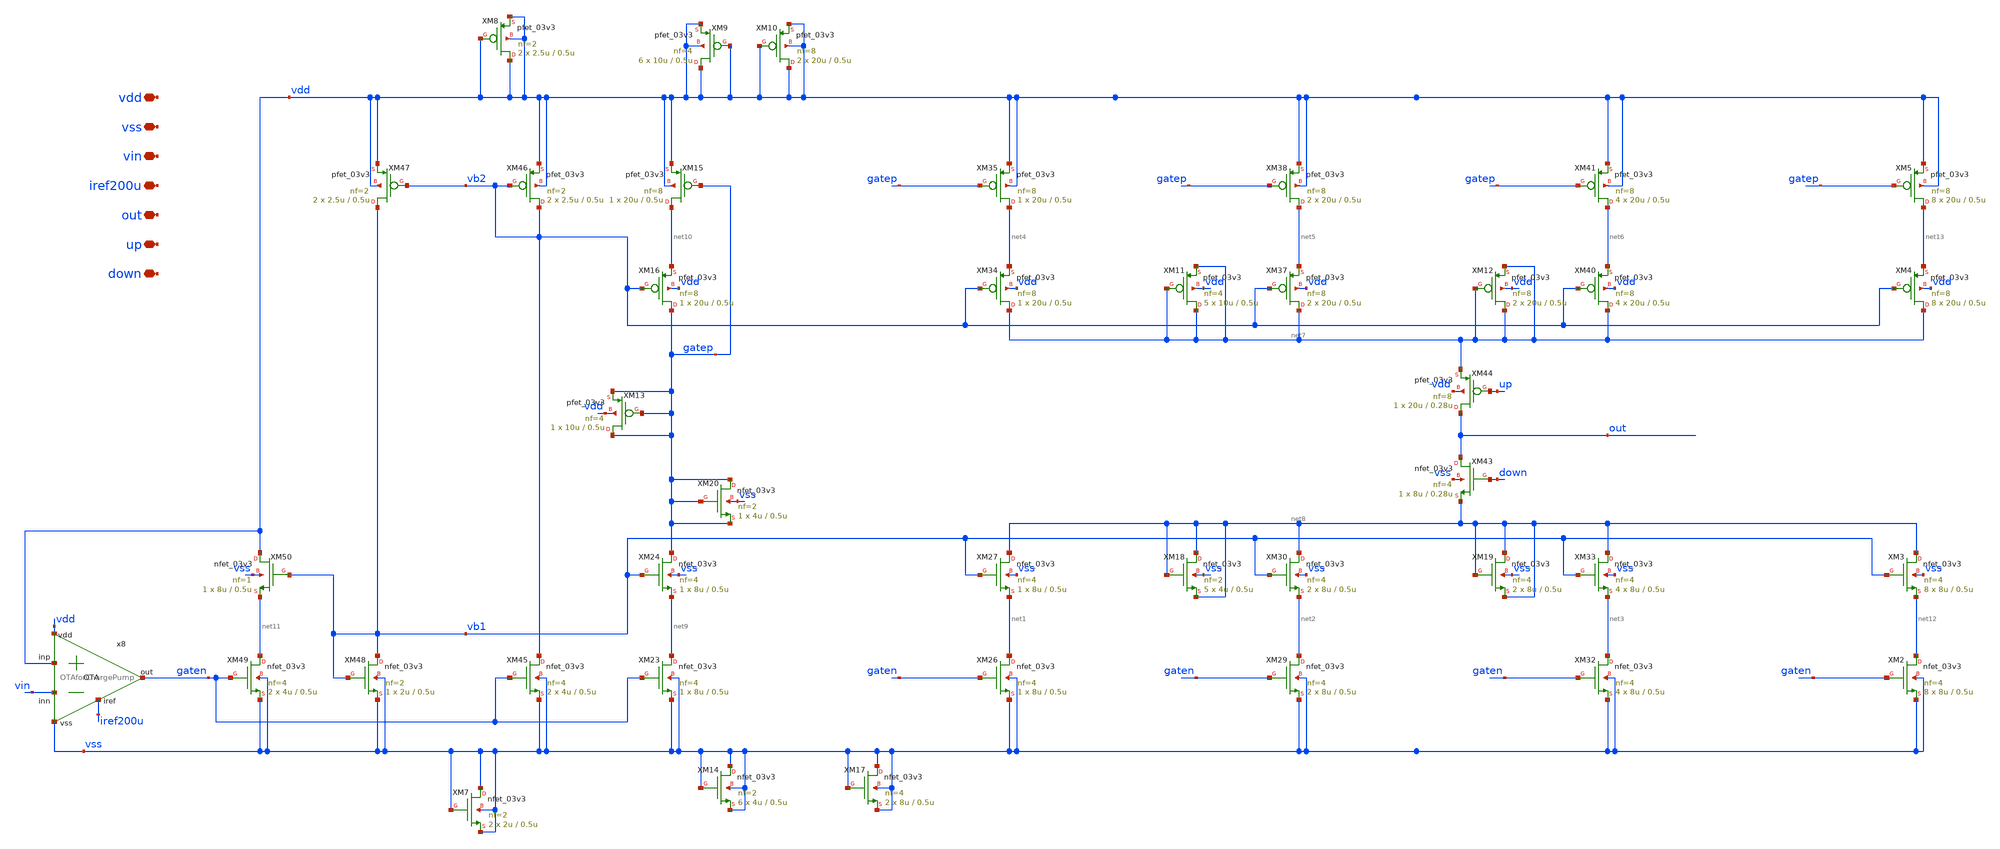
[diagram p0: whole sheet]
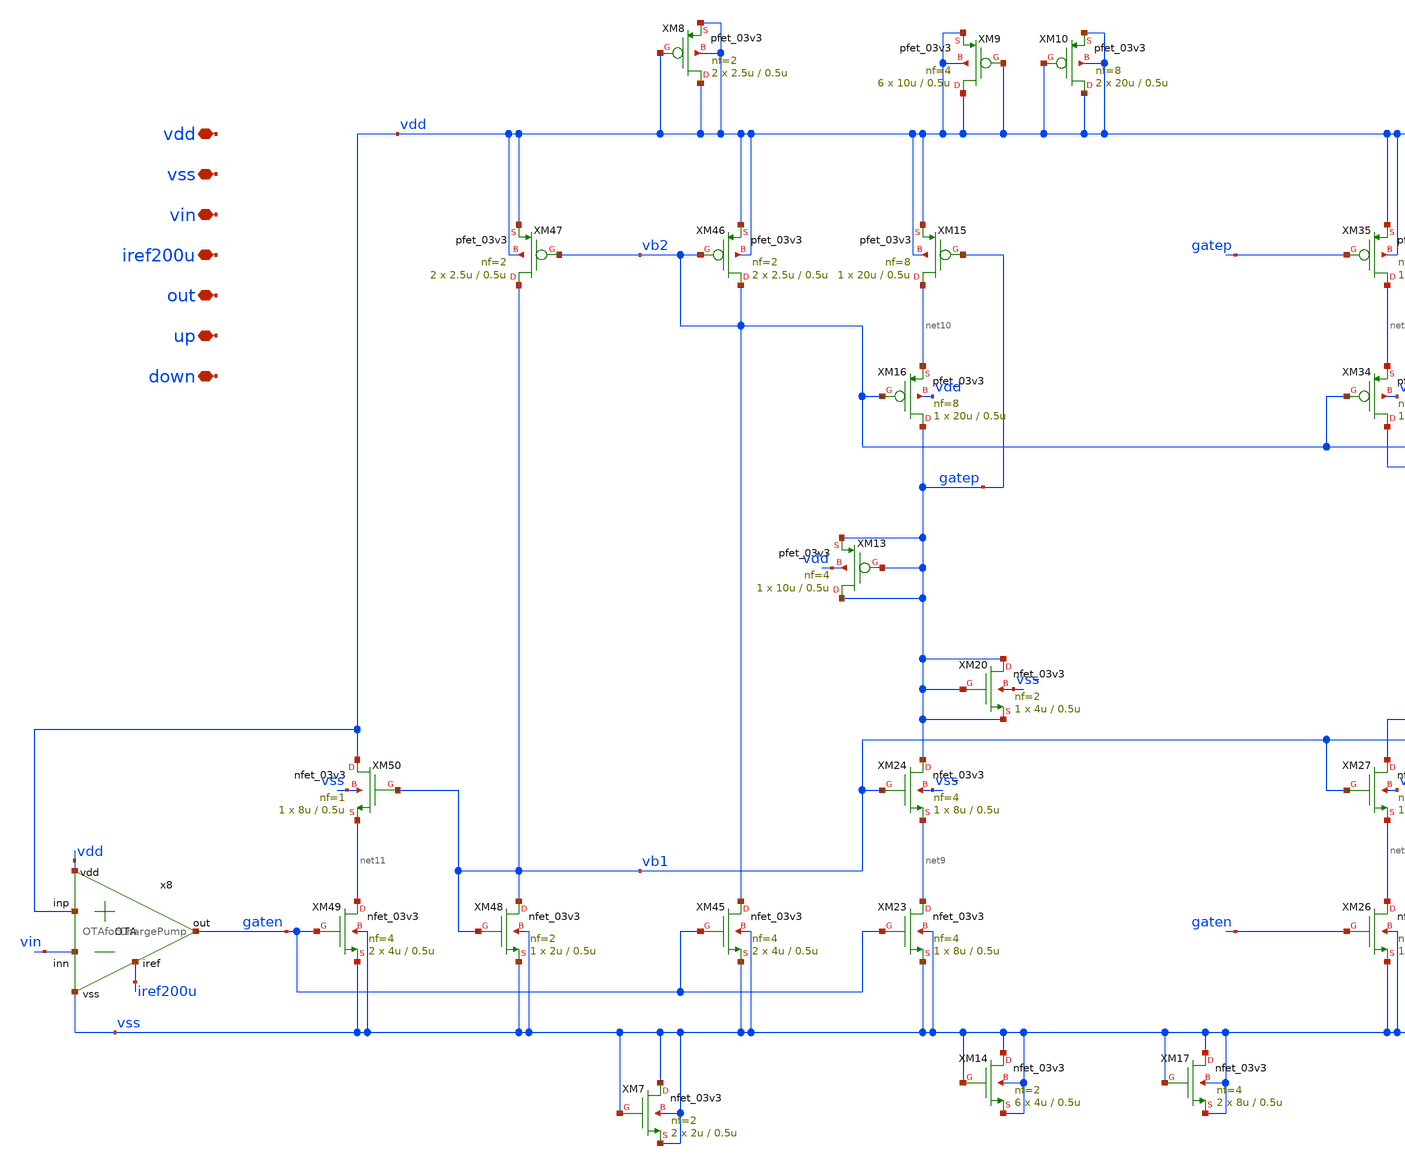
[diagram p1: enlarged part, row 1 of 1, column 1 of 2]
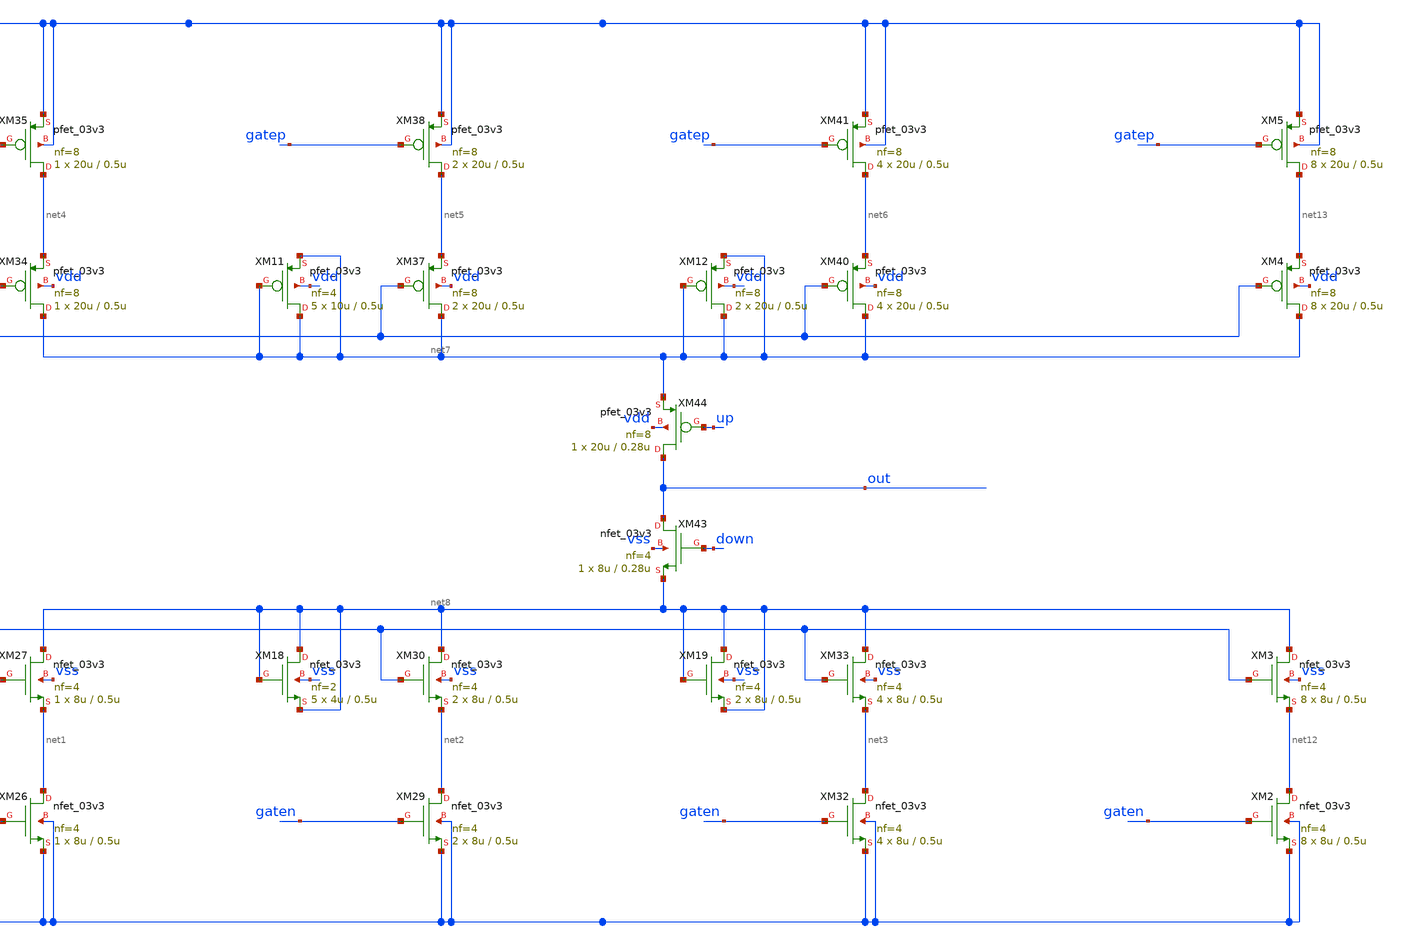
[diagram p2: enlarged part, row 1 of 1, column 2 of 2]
** sch_path: designs/libs/qw_core_analog/PCP15XnoTG/PCP15XnoTG.sch
**.subckt PCP15XnoTG vdd vss vin iref200u out up down
*.iopin vdd
*.iopin vss
*.iopin vin
*.iopin iref200u
*.iopin out
*.iopin up
*.iopin down
XM26 net1 gaten vss vss nfet_03v3 L=0.5u W=8u nf=4 ad='int((nf+1)/2) * W/nf * 0.18u' as='int((nf+2)/2) * W/nf * 0.18u'
+ pd='2*int((nf+1)/2) * (W/nf + 0.18u)' ps='2*int((nf+2)/2) * (W/nf + 0.18u)' nrd='0.18u / W' nrs='0.18u / W'
+ sa=0 sb=0 sd=0 m=1
XM27 net8 vb1 net1 vss nfet_03v3 L=0.5u W=8u nf=4 ad='int((nf+1)/2) * W/nf * 0.18u' as='int((nf+2)/2) * W/nf * 0.18u'
+ pd='2*int((nf+1)/2) * (W/nf + 0.18u)' ps='2*int((nf+2)/2) * (W/nf + 0.18u)' nrd='0.18u / W' nrs='0.18u / W'
+ sa=0 sb=0 sd=0 m=1
XM29 net2 gaten vss vss nfet_03v3 L=0.5u W=8u nf=4 ad='int((nf+1)/2) * W/nf * 0.18u' as='int((nf+2)/2) * W/nf * 0.18u'
+ pd='2*int((nf+1)/2) * (W/nf + 0.18u)' ps='2*int((nf+2)/2) * (W/nf + 0.18u)' nrd='0.18u / W' nrs='0.18u / W'
+ sa=0 sb=0 sd=0 m=2
XM30 net8 vb1 net2 vss nfet_03v3 L=0.5u W=8u nf=4 ad='int((nf+1)/2) * W/nf * 0.18u' as='int((nf+2)/2) * W/nf * 0.18u'
+ pd='2*int((nf+1)/2) * (W/nf + 0.18u)' ps='2*int((nf+2)/2) * (W/nf + 0.18u)' nrd='0.18u / W' nrs='0.18u / W'
+ sa=0 sb=0 sd=0 m=2
XM32 net3 gaten vss vss nfet_03v3 L=0.5u W=8u nf=4 ad='int((nf+1)/2) * W/nf * 0.18u' as='int((nf+2)/2) * W/nf * 0.18u'
+ pd='2*int((nf+1)/2) * (W/nf + 0.18u)' ps='2*int((nf+2)/2) * (W/nf + 0.18u)' nrd='0.18u / W' nrs='0.18u / W'
+ sa=0 sb=0 sd=0 m=4
XM33 net8 vb1 net3 vss nfet_03v3 L=0.5u W=8u nf=4 ad='int((nf+1)/2) * W/nf * 0.18u' as='int((nf+2)/2) * W/nf * 0.18u'
+ pd='2*int((nf+1)/2) * (W/nf + 0.18u)' ps='2*int((nf+2)/2) * (W/nf + 0.18u)' nrd='0.18u / W' nrs='0.18u / W'
+ sa=0 sb=0 sd=0 m=4
XM34 net7 vb2 net4 vdd pfet_03v3 L=0.5u W=20u nf=8 ad='int((nf+1)/2) * W/nf * 0.18u' as='int((nf+2)/2) * W/nf * 0.18u'
+ pd='2*int((nf+1)/2) * (W/nf + 0.18u)' ps='2*int((nf+2)/2) * (W/nf + 0.18u)' nrd='0.18u / W' nrs='0.18u / W'
+ sa=0 sb=0 sd=0 m=1
XM35 net4 gatep vdd vdd pfet_03v3 L=0.5u W=20u nf=8 ad='int((nf+1)/2) * W/nf * 0.18u' as='int((nf+2)/2) * W/nf * 0.18u'
+ pd='2*int((nf+1)/2) * (W/nf + 0.18u)' ps='2*int((nf+2)/2) * (W/nf + 0.18u)' nrd='0.18u / W' nrs='0.18u / W'
+ sa=0 sb=0 sd=0 m=1
XM37 net7 vb2 net5 vdd pfet_03v3 L=0.5u W=20u nf=8 ad='int((nf+1)/2) * W/nf * 0.18u' as='int((nf+2)/2) * W/nf * 0.18u'
+ pd='2*int((nf+1)/2) * (W/nf + 0.18u)' ps='2*int((nf+2)/2) * (W/nf + 0.18u)' nrd='0.18u / W' nrs='0.18u / W'
+ sa=0 sb=0 sd=0 m=2
XM38 net5 gatep vdd vdd pfet_03v3 L=0.5u W=20u nf=8 ad='int((nf+1)/2) * W/nf * 0.18u' as='int((nf+2)/2) * W/nf * 0.18u'
+ pd='2*int((nf+1)/2) * (W/nf + 0.18u)' ps='2*int((nf+2)/2) * (W/nf + 0.18u)' nrd='0.18u / W' nrs='0.18u / W'
+ sa=0 sb=0 sd=0 m=2
XM40 net7 vb2 net6 vdd pfet_03v3 L=0.5u W=20u nf=8 ad='int((nf+1)/2) * W/nf * 0.18u' as='int((nf+2)/2) * W/nf * 0.18u'
+ pd='2*int((nf+1)/2) * (W/nf + 0.18u)' ps='2*int((nf+2)/2) * (W/nf + 0.18u)' nrd='0.18u / W' nrs='0.18u / W'
+ sa=0 sb=0 sd=0 m=4
XM41 net6 gatep vdd vdd pfet_03v3 L=0.5u W=20u nf=8 ad='int((nf+1)/2) * W/nf * 0.18u' as='int((nf+2)/2) * W/nf * 0.18u'
+ pd='2*int((nf+1)/2) * (W/nf + 0.18u)' ps='2*int((nf+2)/2) * (W/nf + 0.18u)' nrd='0.18u / W' nrs='0.18u / W'
+ sa=0 sb=0 sd=0 m=4
XM43 out down net8 vss nfet_03v3 L=0.28u W=8u nf=4 ad='int((nf+1)/2) * W/nf * 0.18u' as='int((nf+2)/2) * W/nf * 0.18u'
+ pd='2*int((nf+1)/2) * (W/nf + 0.18u)' ps='2*int((nf+2)/2) * (W/nf + 0.18u)' nrd='0.18u / W' nrs='0.18u / W'
+ sa=0 sb=0 sd=0 m=1
XM44 out up net7 vdd pfet_03v3 L=0.28u W=20u nf=8 ad='int((nf+1)/2) * W/nf * 0.18u' as='int((nf+2)/2) * W/nf * 0.18u'
+ pd='2*int((nf+1)/2) * (W/nf + 0.18u)' ps='2*int((nf+2)/2) * (W/nf + 0.18u)' nrd='0.18u / W' nrs='0.18u / W'
+ sa=0 sb=0 sd=0 m=1
XM15 net10 gatep vdd vdd pfet_03v3 L=0.5u W=20u nf=8 ad='int((nf+1)/2) * W/nf * 0.18u' as='int((nf+2)/2) * W/nf * 0.18u'
+ pd='2*int((nf+1)/2) * (W/nf + 0.18u)' ps='2*int((nf+2)/2) * (W/nf + 0.18u)' nrd='0.18u / W' nrs='0.18u / W'
+ sa=0 sb=0 sd=0 m=1
XM16 gatep vb2 net10 vdd pfet_03v3 L=0.5u W=20u nf=8 ad='int((nf+1)/2) * W/nf * 0.18u' as='int((nf+2)/2) * W/nf * 0.18u'
+ pd='2*int((nf+1)/2) * (W/nf + 0.18u)' ps='2*int((nf+2)/2) * (W/nf + 0.18u)' nrd='0.18u / W' nrs='0.18u / W'
+ sa=0 sb=0 sd=0 m=1
XM23 net9 gaten vss vss nfet_03v3 L=0.5u W=8u nf=4 ad='int((nf+1)/2) * W/nf * 0.18u' as='int((nf+2)/2) * W/nf * 0.18u'
+ pd='2*int((nf+1)/2) * (W/nf + 0.18u)' ps='2*int((nf+2)/2) * (W/nf + 0.18u)' nrd='0.18u / W' nrs='0.18u / W'
+ sa=0 sb=0 sd=0 m=1
XM24 gatep vb1 net9 vss nfet_03v3 L=0.5u W=8u nf=4 ad='int((nf+1)/2) * W/nf * 0.18u' as='int((nf+2)/2) * W/nf * 0.18u'
+ pd='2*int((nf+1)/2) * (W/nf + 0.18u)' ps='2*int((nf+2)/2) * (W/nf + 0.18u)' nrd='0.18u / W' nrs='0.18u / W'
+ sa=0 sb=0 sd=0 m=1
XM45 vb2 gaten vss vss nfet_03v3 L=0.5u W=4u nf=4 ad='int((nf+1)/2) * W/nf * 0.18u' as='int((nf+2)/2) * W/nf * 0.18u'
+ pd='2*int((nf+1)/2) * (W/nf + 0.18u)' ps='2*int((nf+2)/2) * (W/nf + 0.18u)' nrd='0.18u / W' nrs='0.18u / W'
+ sa=0 sb=0 sd=0 m=2
XM46 vb2 vb2 vdd vdd pfet_03v3 L=0.5u W=2.5u nf=2 ad='int((nf+1)/2) * W/nf * 0.18u' as='int((nf+2)/2) * W/nf * 0.18u'
+ pd='2*int((nf+1)/2) * (W/nf + 0.18u)' ps='2*int((nf+2)/2) * (W/nf + 0.18u)' nrd='0.18u / W' nrs='0.18u / W'
+ sa=0 sb=0 sd=0 m=2
XM47 vb1 vb2 vdd vdd pfet_03v3 L=0.5u W=2.5u nf=2 ad='int((nf+1)/2) * W/nf * 0.18u' as='int((nf+2)/2) * W/nf * 0.18u'
+ pd='2*int((nf+1)/2) * (W/nf + 0.18u)' ps='2*int((nf+2)/2) * (W/nf + 0.18u)' nrd='0.18u / W' nrs='0.18u / W'
+ sa=0 sb=0 sd=0 m=2
XM48 vb1 vb1 vss vss nfet_03v3 L=0.5u W=2u nf=2 ad='int((nf+1)/2) * W/nf * 0.18u' as='int((nf+2)/2) * W/nf * 0.18u'
+ pd='2*int((nf+1)/2) * (W/nf + 0.18u)' ps='2*int((nf+2)/2) * (W/nf + 0.18u)' nrd='0.18u / W' nrs='0.18u / W'
+ sa=0 sb=0 sd=0 m=1
XM49 net11 gaten vss vss nfet_03v3 L=0.5u W=4u nf=4 ad='int((nf+1)/2) * W/nf * 0.18u' as='int((nf+2)/2) * W/nf * 0.18u'
+ pd='2*int((nf+1)/2) * (W/nf + 0.18u)' ps='2*int((nf+2)/2) * (W/nf + 0.18u)' nrd='0.18u / W' nrs='0.18u / W'
+ sa=0 sb=0 sd=0 m=2
XM50 vdd vb1 net11 vss nfet_03v3 L=0.5u W=8u nf=1 ad='int((nf+1)/2) * W/nf * 0.18u' as='int((nf+2)/2) * W/nf * 0.18u'
+ pd='2*int((nf+1)/2) * (W/nf + 0.18u)' ps='2*int((nf+2)/2) * (W/nf + 0.18u)' nrd='0.18u / W' nrs='0.18u / W'
+ sa=0 sb=0 sd=0 m=1
x8 vdd iref200u vdd vin gaten vss OTAforChargePump
XM2 net12 gaten vss vss nfet_03v3 L=0.5u W=8u nf=4 ad='int((nf+1)/2) * W/nf * 0.18u' as='int((nf+2)/2) * W/nf * 0.18u'
+ pd='2*int((nf+1)/2) * (W/nf + 0.18u)' ps='2*int((nf+2)/2) * (W/nf + 0.18u)' nrd='0.18u / W' nrs='0.18u / W'
+ sa=0 sb=0 sd=0 m=8
XM3 net8 vb1 net12 vss nfet_03v3 L=0.5u W=8u nf=4 ad='int((nf+1)/2) * W/nf * 0.18u' as='int((nf+2)/2) * W/nf * 0.18u'
+ pd='2*int((nf+1)/2) * (W/nf + 0.18u)' ps='2*int((nf+2)/2) * (W/nf + 0.18u)' nrd='0.18u / W' nrs='0.18u / W'
+ sa=0 sb=0 sd=0 m=8
XM4 net7 vb2 net13 vdd pfet_03v3 L=0.5u W=20u nf=8 ad='int((nf+1)/2) * W/nf * 0.18u' as='int((nf+2)/2) * W/nf * 0.18u'
+ pd='2*int((nf+1)/2) * (W/nf + 0.18u)' ps='2*int((nf+2)/2) * (W/nf + 0.18u)' nrd='0.18u / W' nrs='0.18u / W'
+ sa=0 sb=0 sd=0 m=8
XM5 net13 gatep vdd vdd pfet_03v3 L=0.5u W=20u nf=8 ad='int((nf+1)/2) * W/nf * 0.18u' as='int((nf+2)/2) * W/nf * 0.18u'
+ pd='2*int((nf+1)/2) * (W/nf + 0.18u)' ps='2*int((nf+2)/2) * (W/nf + 0.18u)' nrd='0.18u / W' nrs='0.18u / W'
+ sa=0 sb=0 sd=0 m=8
XM7 vss vss vss vss nfet_03v3 L=0.5u W=2u nf=2 ad='int((nf+1)/2) * W/nf * 0.18u' as='int((nf+2)/2) * W/nf * 0.18u'
+ pd='2*int((nf+1)/2) * (W/nf + 0.18u)' ps='2*int((nf+2)/2) * (W/nf + 0.18u)' nrd='0.18u / W' nrs='0.18u / W'
+ sa=0 sb=0 sd=0 m=2
XM8 vdd vdd vdd vdd pfet_03v3 L=0.5u W=2.5u nf=2 ad='int((nf+1)/2) * W/nf * 0.18u' as='int((nf+2)/2) * W/nf * 0.18u'
+ pd='2*int((nf+1)/2) * (W/nf + 0.18u)' ps='2*int((nf+2)/2) * (W/nf + 0.18u)' nrd='0.18u / W' nrs='0.18u / W'
+ sa=0 sb=0 sd=0 m=2
XM9 vdd vdd vdd vdd pfet_03v3 L=0.5u W=10u nf=4 ad='int((nf+1)/2) * W/nf * 0.18u' as='int((nf+2)/2) * W/nf * 0.18u'
+ pd='2*int((nf+1)/2) * (W/nf + 0.18u)' ps='2*int((nf+2)/2) * (W/nf + 0.18u)' nrd='0.18u / W' nrs='0.18u / W'
+ sa=0 sb=0 sd=0 m=6
XM10 vdd vdd vdd vdd pfet_03v3 L=0.5u W=20u nf=8 ad='int((nf+1)/2) * W/nf * 0.18u' as='int((nf+2)/2) * W/nf * 0.18u'
+ pd='2*int((nf+1)/2) * (W/nf + 0.18u)' ps='2*int((nf+2)/2) * (W/nf + 0.18u)' nrd='0.18u / W' nrs='0.18u / W'
+ sa=0 sb=0 sd=0 m=2
XM11 net7 net7 net7 vdd pfet_03v3 L=0.5u W=10u nf=4 ad='int((nf+1)/2) * W/nf * 0.18u' as='int((nf+2)/2) * W/nf * 0.18u'
+ pd='2*int((nf+1)/2) * (W/nf + 0.18u)' ps='2*int((nf+2)/2) * (W/nf + 0.18u)' nrd='0.18u / W' nrs='0.18u / W'
+ sa=0 sb=0 sd=0 m=5
XM12 net7 net7 net7 vdd pfet_03v3 L=0.5u W=20u nf=8 ad='int((nf+1)/2) * W/nf * 0.18u' as='int((nf+2)/2) * W/nf * 0.18u'
+ pd='2*int((nf+1)/2) * (W/nf + 0.18u)' ps='2*int((nf+2)/2) * (W/nf + 0.18u)' nrd='0.18u / W' nrs='0.18u / W'
+ sa=0 sb=0 sd=0 m=2
XM13 gatep gatep gatep vdd pfet_03v3 L=0.5u W=10u nf=4 ad='int((nf+1)/2) * W/nf * 0.18u' as='int((nf+2)/2) * W/nf * 0.18u'
+ pd='2*int((nf+1)/2) * (W/nf + 0.18u)' ps='2*int((nf+2)/2) * (W/nf + 0.18u)' nrd='0.18u / W' nrs='0.18u / W'
+ sa=0 sb=0 sd=0 m=1
XM14 vss vss vss vss nfet_03v3 L=0.5u W=4u nf=2 ad='int((nf+1)/2) * W/nf * 0.18u' as='int((nf+2)/2) * W/nf * 0.18u'
+ pd='2*int((nf+1)/2) * (W/nf + 0.18u)' ps='2*int((nf+2)/2) * (W/nf + 0.18u)' nrd='0.18u / W' nrs='0.18u / W'
+ sa=0 sb=0 sd=0 m=6
XM17 vss vss vss vss nfet_03v3 L=0.5u W=8u nf=4 ad='int((nf+1)/2) * W/nf * 0.18u' as='int((nf+2)/2) * W/nf * 0.18u'
+ pd='2*int((nf+1)/2) * (W/nf + 0.18u)' ps='2*int((nf+2)/2) * (W/nf + 0.18u)' nrd='0.18u / W' nrs='0.18u / W'
+ sa=0 sb=0 sd=0 m=2
XM18 net8 net8 net8 vss nfet_03v3 L=0.5u W=4u nf=2 ad='int((nf+1)/2) * W/nf * 0.18u' as='int((nf+2)/2) * W/nf * 0.18u'
+ pd='2*int((nf+1)/2) * (W/nf + 0.18u)' ps='2*int((nf+2)/2) * (W/nf + 0.18u)' nrd='0.18u / W' nrs='0.18u / W'
+ sa=0 sb=0 sd=0 m=5
XM19 net8 net8 net8 vss nfet_03v3 L=0.5u W=8u nf=4 ad='int((nf+1)/2) * W/nf * 0.18u' as='int((nf+2)/2) * W/nf * 0.18u'
+ pd='2*int((nf+1)/2) * (W/nf + 0.18u)' ps='2*int((nf+2)/2) * (W/nf + 0.18u)' nrd='0.18u / W' nrs='0.18u / W'
+ sa=0 sb=0 sd=0 m=2
XM20 gatep gatep gatep vss nfet_03v3 L=0.5u W=4u nf=2 ad='int((nf+1)/2) * W/nf * 0.18u' as='int((nf+2)/2) * W/nf * 0.18u'
+ pd='2*int((nf+1)/2) * (W/nf + 0.18u)' ps='2*int((nf+2)/2) * (W/nf + 0.18u)' nrd='0.18u / W' nrs='0.18u / W'
+ sa=0 sb=0 sd=0 m=1
**.ends

* expanding   symbol:  libs/qw_core_analog/OTAforChargePump/OTAforChargePump.sym # of pins=6
** sym_path: designs/libs/qw_core_analog_pkedit/OTAforChargePump/OTAforChargePump.sym
** sch_path: designs/libs/qw_core_analog_pkedit/OTAforChargePump/OTAforChargePump.sch
.subckt OTAforChargePump vdd iref inp inn out vss
*.iopin inp
*.iopin inn
*.iopin vdd
*.iopin vss
*.iopin out
*.iopin iref
XM8 iref iref vdd vdd pfet_03v3 L=0.28u W=40u nf=1 ad='int((nf+1)/2) * W/nf * 0.18u' as='int((nf+2)/2) * W/nf * 0.18u'
+ pd='2*int((nf+1)/2) * (W/nf + 0.18u)' ps='2*int((nf+2)/2) * (W/nf + 0.18u)' nrd='0.18u / W' nrs='0.18u / W'
+ sa=0 sb=0 sd=0 m=1
XM1 net1 iref vdd vdd pfet_03v3 L=0.28u W=40u nf=1 ad='int((nf+1)/2) * W/nf * 0.18u' as='int((nf+2)/2) * W/nf * 0.18u'
+ pd='2*int((nf+1)/2) * (W/nf + 0.18u)' ps='2*int((nf+2)/2) * (W/nf + 0.18u)' nrd='0.18u / W' nrs='0.18u / W'
+ sa=0 sb=0 sd=0 m=1
XM2 net2 inp net1 vdd pfet_03v3 L=0.28u W=20u nf=1 ad='int((nf+1)/2) * W/nf * 0.18u' as='int((nf+2)/2) * W/nf * 0.18u'
+ pd='2*int((nf+1)/2) * (W/nf + 0.18u)' ps='2*int((nf+2)/2) * (W/nf + 0.18u)' nrd='0.18u / W' nrs='0.18u / W'
+ sa=0 sb=0 sd=0 m=1
XM3 out inn net1 vdd pfet_03v3 L=0.28u W=20u nf=1 ad='int((nf+1)/2) * W/nf * 0.18u' as='int((nf+2)/2) * W/nf * 0.18u'
+ pd='2*int((nf+1)/2) * (W/nf + 0.18u)' ps='2*int((nf+2)/2) * (W/nf + 0.18u)' nrd='0.18u / W' nrs='0.18u / W'
+ sa=0 sb=0 sd=0 m=1
XM4 net2 net2 vss vss nfet_03v3 L=0.28u W=8u nf=1 ad='int((nf+1)/2) * W/nf * 0.18u' as='int((nf+2)/2) * W/nf * 0.18u'
+ pd='2*int((nf+1)/2) * (W/nf + 0.18u)' ps='2*int((nf+2)/2) * (W/nf + 0.18u)' nrd='0.18u / W' nrs='0.18u / W'
+ sa=0 sb=0 sd=0 m=1
XM5 out net2 vss vss nfet_03v3 L=0.28u W=8u nf=1 ad='int((nf+1)/2) * W/nf * 0.18u' as='int((nf+2)/2) * W/nf * 0.18u'
+ pd='2*int((nf+1)/2) * (W/nf + 0.18u)' ps='2*int((nf+2)/2) * (W/nf + 0.18u)' nrd='0.18u / W' nrs='0.18u / W'
+ sa=0 sb=0 sd=0 m=1
.ends

.end
